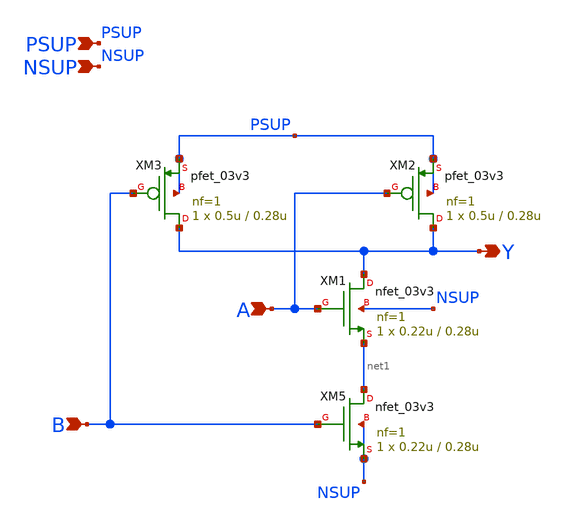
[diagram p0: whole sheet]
** sch_path: xschem/blocks/nand_2/nand_2.sch
**.subckt nand_2 PSUP NSUP A B Y
*.ipin PSUP
*.ipin NSUP
*.ipin A
*.ipin B
*.opin Y
XM5 net1 B NSUP NSUP nfet_03v3 L=0.28u W=0.22u nf=1 ad='int((nf+1)/2) * W/nf * 0.18u' as='int((nf+2)/2) * W/nf * 0.18u'
+ pd='2*int((nf+1)/2) * (W/nf + 0.18u)' ps='2*int((nf+2)/2) * (W/nf + 0.18u)' nrd='0.18u / W' nrs='0.18u / W'
+ sa=0 sb=0 sd=0 m=1
XM1 Y A net1 NSUP nfet_03v3 L=0.28u W=0.22u nf=1 ad='int((nf+1)/2) * W/nf * 0.18u' as='int((nf+2)/2) * W/nf * 0.18u'
+ pd='2*int((nf+1)/2) * (W/nf + 0.18u)' ps='2*int((nf+2)/2) * (W/nf + 0.18u)' nrd='0.18u / W' nrs='0.18u / W'
+ sa=0 sb=0 sd=0 m=1
XM2 Y A PSUP PSUP pfet_03v3 L=0.28u W=0.5u nf=1 ad='int((nf+1)/2) * W/nf * 0.18u' as='int((nf+2)/2) * W/nf * 0.18u'
+ pd='2*int((nf+1)/2) * (W/nf + 0.18u)' ps='2*int((nf+2)/2) * (W/nf + 0.18u)' nrd='0.18u / W' nrs='0.18u / W'
+ sa=0 sb=0 sd=0 m=1
XM3 Y B PSUP PSUP pfet_03v3 L=0.28u W=0.5u nf=1 ad='int((nf+1)/2) * W/nf * 0.18u' as='int((nf+2)/2) * W/nf * 0.18u'
+ pd='2*int((nf+1)/2) * (W/nf + 0.18u)' ps='2*int((nf+2)/2) * (W/nf + 0.18u)' nrd='0.18u / W' nrs='0.18u / W'
+ sa=0 sb=0 sd=0 m=1
**.ends
.end
